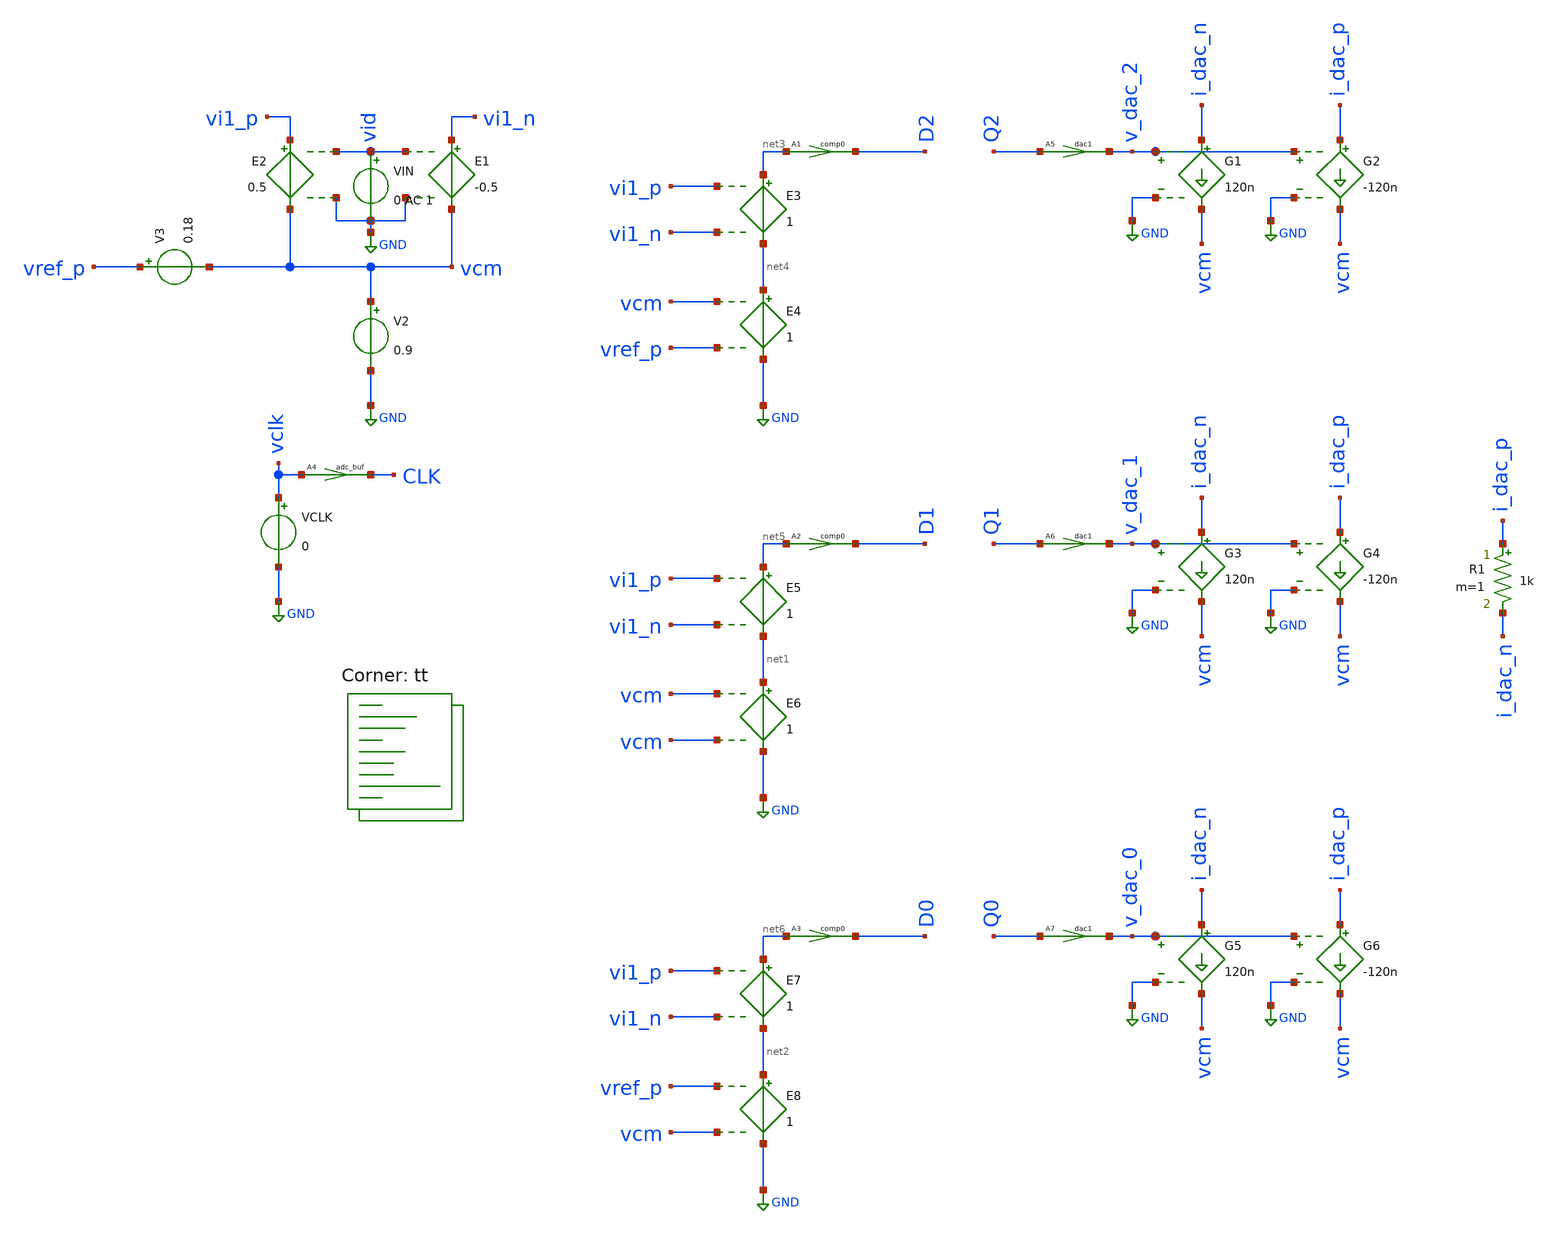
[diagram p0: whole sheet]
** sch_path: circuit-level/xschem/macro-models/adc_dac_macro.sch
**.subckt adc_dac_macro
A1 [ net3 ] [ D2 ] comp0
V2 vcm GND 0.9
E1 vi1_n vcm vid GND -0.5
E2 vi1_p vcm vid GND 0.5
VIN vid GND 0 AC 1
VCLK vclk GND 0
V3 vref_p vcm 0.18
E3 net3 net4 vi1_p vi1_n 1
E4 net4 GND vcm vref_p 1
A2 [ net5 ] [ D1 ] comp0
E5 net5 net1 vi1_p vi1_n 1
E6 net1 GND vcm vcm 1
A3 [ net6 ] [ D0 ] comp0
E7 net6 net2 vi1_p vi1_n 1
E8 net2 GND vref_p vcm 1
A4 [ vclk ] [ CLK ] adc_buf
A5 [ Q2 ] [ v_dac_2 ] dac1
A6 [ Q1 ] [ v_dac_1 ] dac1
A7 [ Q0 ] [ v_dac_0 ] dac1
G1 i_dac_n vcm v_dac_2 GND 120n
G2 i_dac_p vcm v_dac_2 GND -120n
G3 i_dac_n vcm v_dac_1 GND 120n
G4 i_dac_p vcm v_dac_1 GND -120n
G5 i_dac_n vcm v_dac_0 GND 120n
G6 i_dac_p vcm v_dac_0 GND -120n
R1 i_dac_p i_dac_n 1k m=1
**** begin user architecture code
.lib $::SKYWATER_MODELS/sky130.lib.spice tt


a21 D0 ND0 inv1
a22 D1 ND1 inv1
a23 D2 ND2 inv1
*a24 D0 ND0 CLK NULL NULL %d(Q0 NQ0) srff1
*a25 D1 ND1 CLK NULL NULL %d(Q1 NQ1) srff1
*a26 D2 ND2 CLK NULL NULL %d(Q2 NQ2) srff1
a24 D0 CLK NULL NULL %d(Q0 NQ0) dff1
a25 D1 CLK NULL NULL %d(Q1 NQ1) dff1
a26 D2 CLK NULL NULL %d(Q2 NQ2) dff1
a27 NQ1 %d(B1) inv1
a28 [NQ1 Q0] temp1 and1
a29 [Q2 temp1] %d(B0) or1


.model comp0 adc_bridge(in_low=-0.0001 in_high=0.0001)
.model adc_buf adc_bridge(in_low=0.899 in_high=0.901)
.model dac1 dac_bridge(out_low = -1 out_high = 1 out_undef = -1 input_load = 5.0e-12 t_rise = 50e-9
+ t_fall = 20e-9)
.model switch1 sw vt=0.9 vh=0.05 ron=0.1 roff=100Meg
.model inv1 d_inverter(rise_delay = 0.5e-9 fall_delay = 0.3e-9 input_load = 0.5e-12)
.model and1 d_and(rise_delay = 0.5e-9 fall_delay = 0.3e-9 input_load = 0.5e-12)
.model or1 d_or(rise_delay = 0.5e-9 fall_delay = 0.3e-9 input_load = 0.5e-12)
.model srff1 d_srff(clk_delay = 13.0e-9 set_delay = 25.0e-9 reset_delay = 27.0e-9 ic = 2 rise_delay
+ = 10.0e-9 fall_delay = 3e-9)
.model dff1 d_dff(clk_delay = 13.0e-9 set_delay = 25.0e-9 reset_delay = 27.0e-9 ic = 0 rise_delay =
+ 10.0e-9 fall_delay = 3e-9)

.options savecurrents
.control
save all


let fs = 65536
let fclk = fs
let tper_clk = 1/fclk
let tfr_clk = tper_clk/10
let ton_clk = tper_clk*4/10

let f_sig = 128
let tper_sig = 1/f_sig
let tfr_sig = tper_sig*5/10
let ton_sig = tper_sig*1/1000

alter @VCLK[PULSE]=[ 0 1.8 0 $&tfr_clk $&tfr_clk $&ton_clk $&tper_clk 0 ]
*alter @VIN[PULSE]=[ -0.36 0.36 0 $&tfr_sig $&tfr_sig $&ton_sig $&tper_sig 0 ]
alter @VIN[SIN] = [ 0 0.36 $&f_sig 0 0 0 ]
alter @VIN[DC] = 0.0

let tstep = 0.005/fclk
let tstop = 1/f_sig
let tstart = 0

** Main Simulations


	*dc VIN -0.36 0.36 0.0001
	tran $&tstep $&tstop $&tstart $&tstep

	*setplot dc1
	*plot D0 D1 D2

	setplot tran1
	let data0 = b0
	let data1 = b1
	let iout = @r1[i]
	let iout_plot = iout*0.125e6
	plot vid D0 D1 D2
	*plot D0 ND0
	plot vid B0 B1 iout_plot
	plot vid v_dac_0 v_dac_1 v_dac_2 iout_plot
	plot iout
	eprvcd B1 B0 D2 D1 D0 > /foss/designs/test_adc.vcd


op


remzerovec
write adc_dac_macro.raw
.endc

**** end user architecture code
**.ends
.GLOBAL GND
.end
